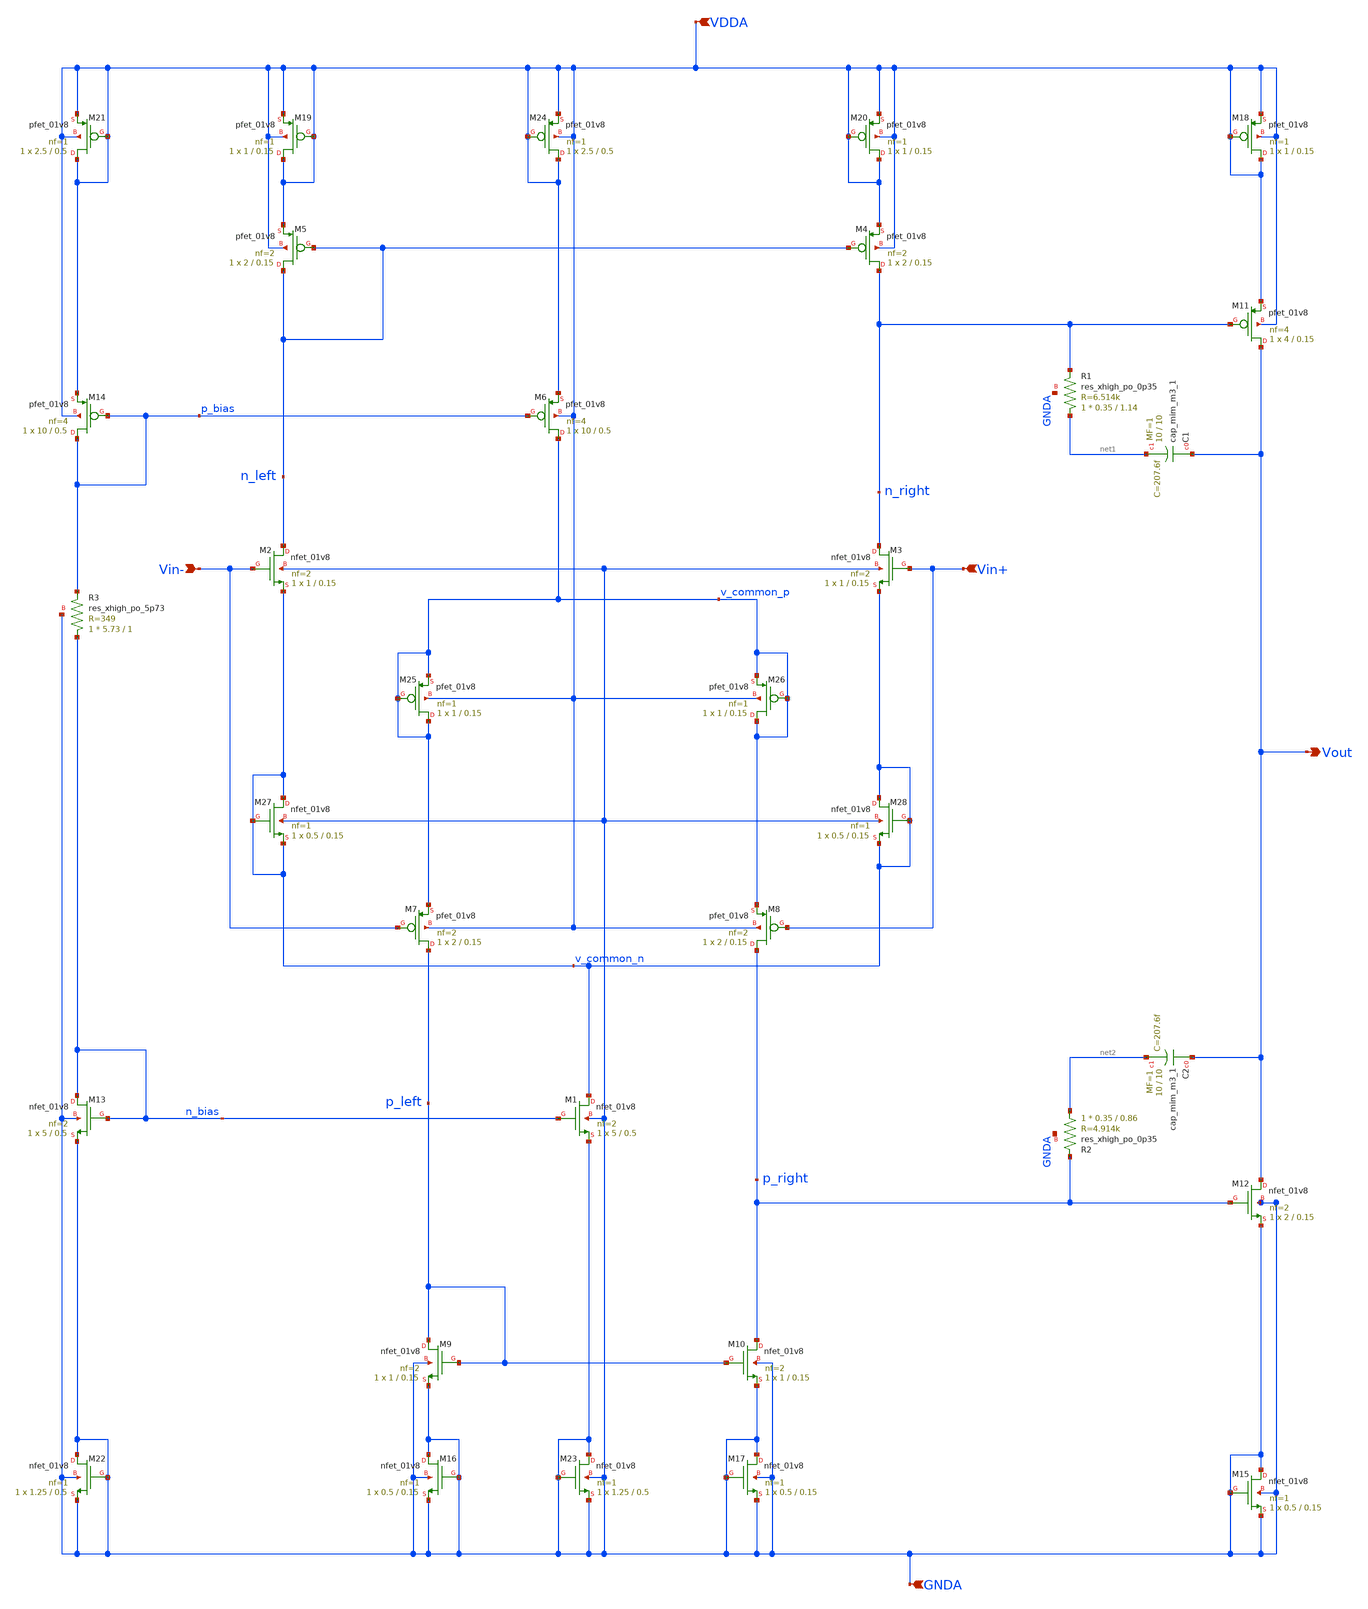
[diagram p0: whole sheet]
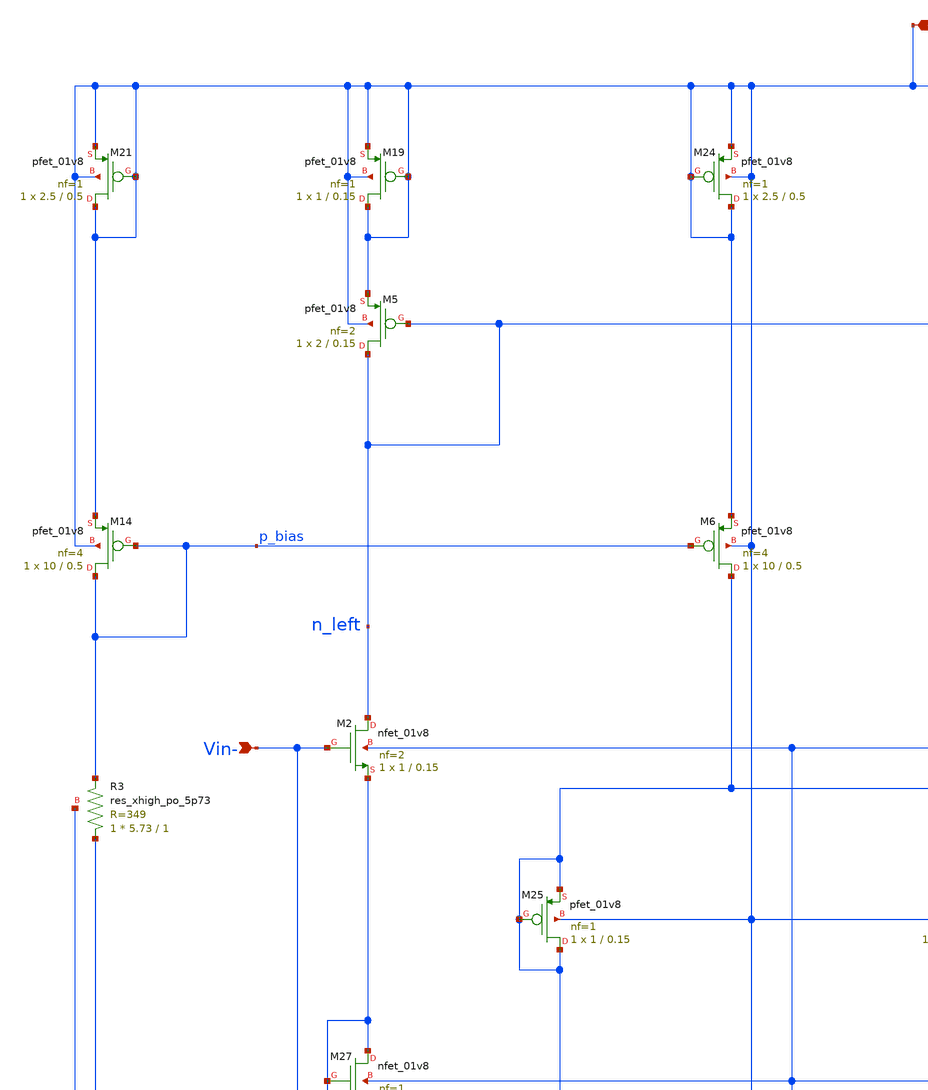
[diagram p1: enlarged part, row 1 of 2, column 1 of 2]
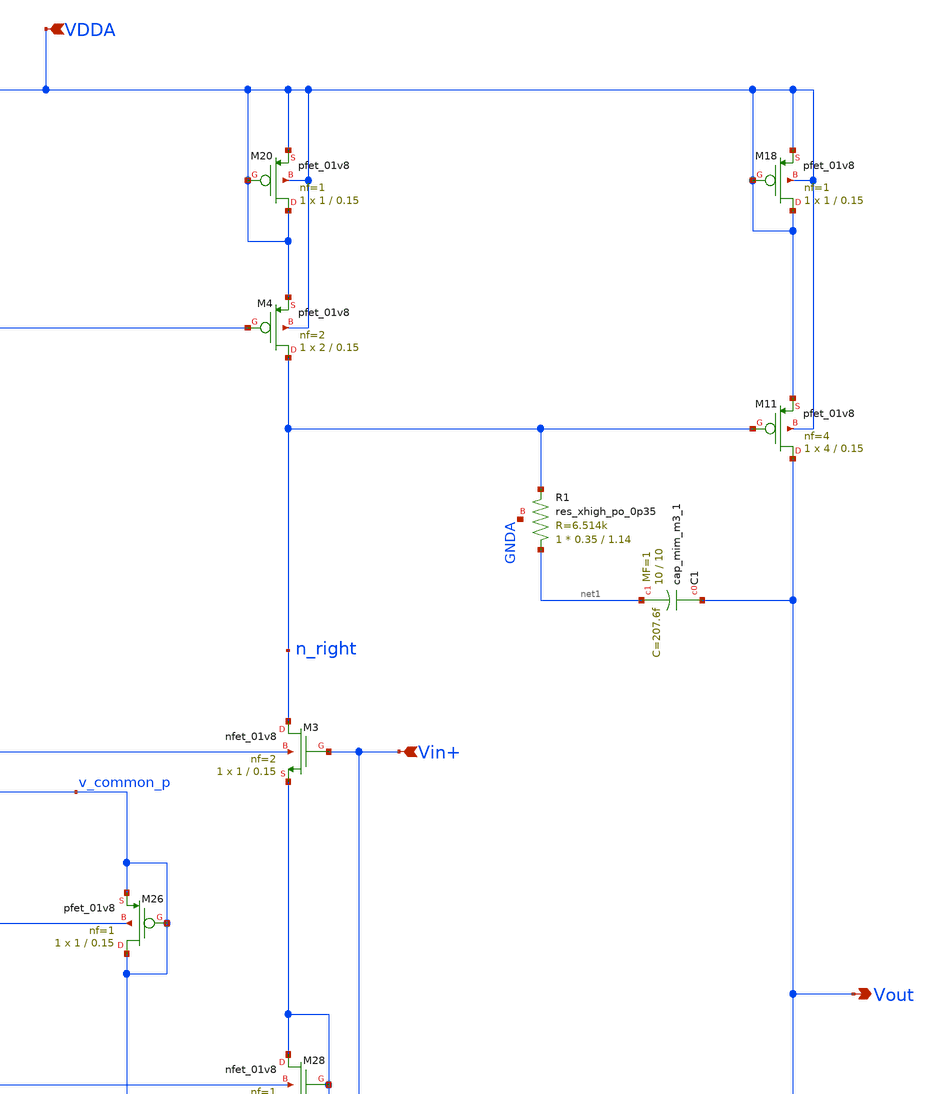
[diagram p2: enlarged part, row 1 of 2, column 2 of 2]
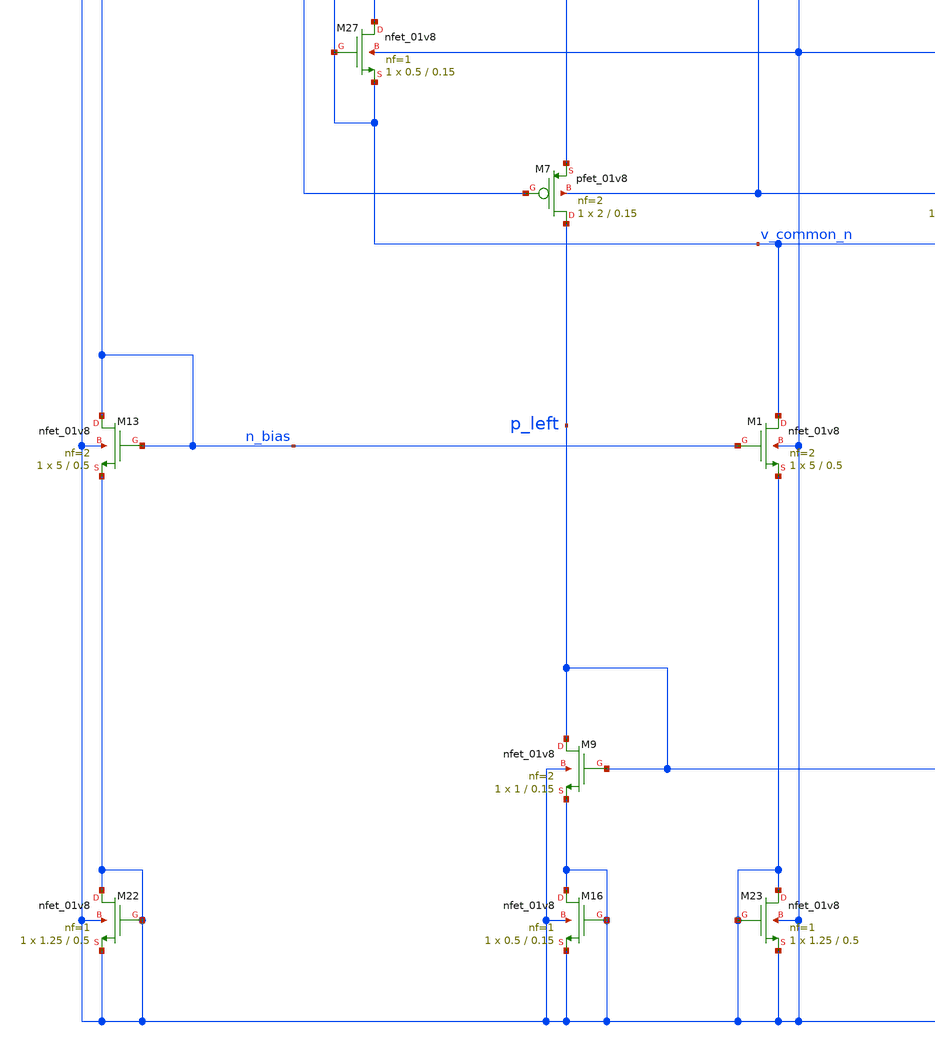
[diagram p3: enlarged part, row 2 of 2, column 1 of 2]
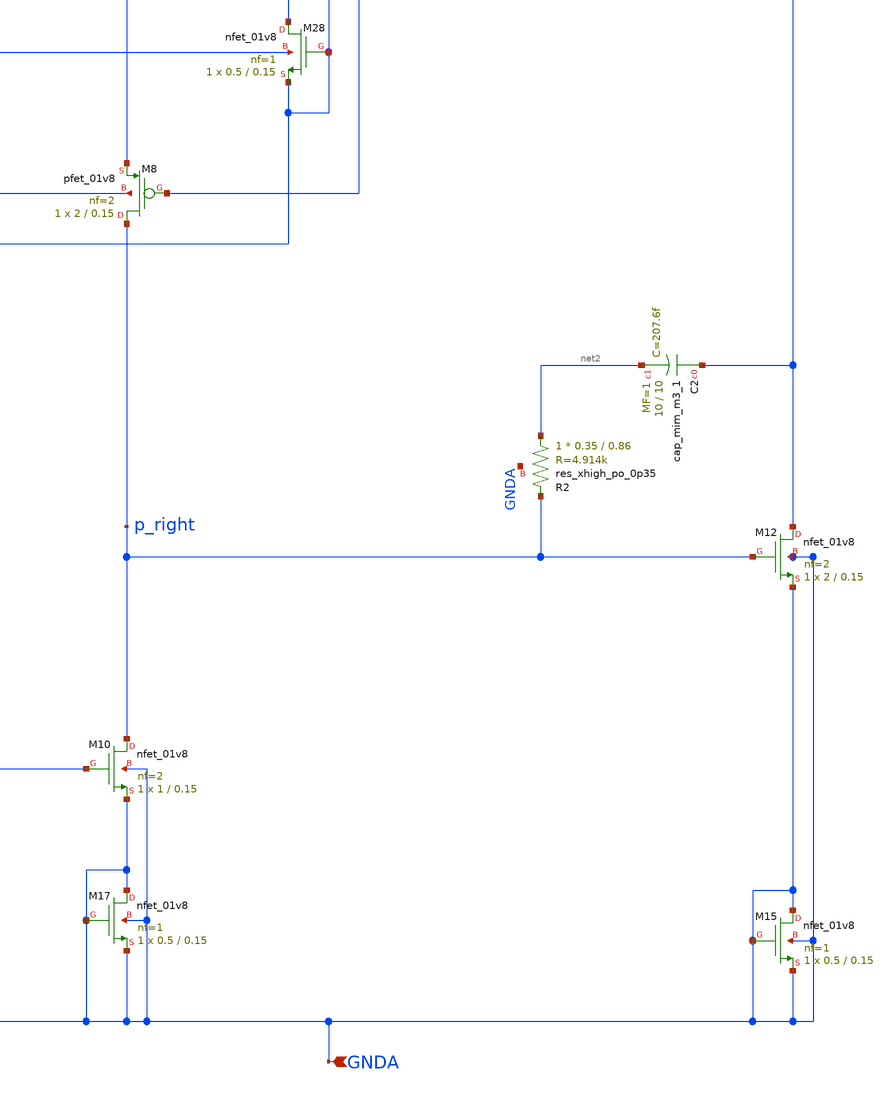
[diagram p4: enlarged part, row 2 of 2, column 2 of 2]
** sch_path: projects/pll/charge_pump/xschem_ngspice/rail_to_rail_opamp6_3.sch
**.subckt rail_to_rail_opamp6_3 Vout Vin+ Vin- VDDA GNDA
*.opin Vout
*.ipin Vin+
*.ipin Vin-
*.ipin VDDA
*.ipin GNDA
XM2 n_left Vin- v_common_n GNDA sky130_fd_pr__nfet_01v8 L=0.15 W=1 nf=2 ad='int((nf+1)/2) * W/nf * 0.29'
+ as='int((nf+2)/2) * W/nf * 0.29' pd='2*int((nf+1)/2) * (W/nf + 0.29)' ps='2*int((nf+2)/2) * (W/nf + 0.29)'
+ nrd='0.29 / W' nrs='0.29 / W' sa=0 sb=0 sd=0 mult=1 m=1
XM3 n_right Vin+ v_common_n GNDA sky130_fd_pr__nfet_01v8 L=0.15 W=1 nf=2 ad='int((nf+1)/2) * W/nf * 0.29'
+ as='int((nf+2)/2) * W/nf * 0.29' pd='2*int((nf+1)/2) * (W/nf + 0.29)' ps='2*int((nf+2)/2) * (W/nf + 0.29)'
+ nrd='0.29 / W' nrs='0.29 / W' sa=0 sb=0 sd=0 mult=1 m=1
XM5 n_left n_left VDDA VDDA sky130_fd_pr__pfet_01v8 L=0.15 W=2 nf=2 ad='int((nf+1)/2) * W/nf * 0.29'
+ as='int((nf+2)/2) * W/nf * 0.29' pd='2*int((nf+1)/2) * (W/nf + 0.29)' ps='2*int((nf+2)/2) * (W/nf + 0.29)'
+ nrd='0.29 / W' nrs='0.29 / W' sa=0 sb=0 sd=0 mult=1 m=1
XM4 n_right n_left VDDA VDDA sky130_fd_pr__pfet_01v8 L=0.15 W=2 nf=2 ad='int((nf+1)/2) * W/nf * 0.29'
+ as='int((nf+2)/2) * W/nf * 0.29' pd='2*int((nf+1)/2) * (W/nf + 0.29)' ps='2*int((nf+2)/2) * (W/nf + 0.29)'
+ nrd='0.29 / W' nrs='0.29 / W' sa=0 sb=0 sd=0 mult=1 m=1
XM6 v_common_p p_bias VDDA VDDA sky130_fd_pr__pfet_01v8 L=0.5 W=10 nf=4 ad='int((nf+1)/2) * W/nf * 0.29'
+ as='int((nf+2)/2) * W/nf * 0.29' pd='2*int((nf+1)/2) * (W/nf + 0.29)' ps='2*int((nf+2)/2) * (W/nf + 0.29)'
+ nrd='0.29 / W' nrs='0.29 / W' sa=0 sb=0 sd=0 mult=1 m=1
XM7 p_left Vin- v_common_p VDDA sky130_fd_pr__pfet_01v8 L=0.15 W=2 nf=2 ad='int((nf+1)/2) * W/nf * 0.29'
+ as='int((nf+2)/2) * W/nf * 0.29' pd='2*int((nf+1)/2) * (W/nf + 0.29)' ps='2*int((nf+2)/2) * (W/nf + 0.29)'
+ nrd='0.29 / W' nrs='0.29 / W' sa=0 sb=0 sd=0 mult=1 m=1
XM8 p_right Vin+ v_common_p VDDA sky130_fd_pr__pfet_01v8 L=0.15 W=2 nf=2 ad='int((nf+1)/2) * W/nf * 0.29'
+ as='int((nf+2)/2) * W/nf * 0.29' pd='2*int((nf+1)/2) * (W/nf + 0.29)' ps='2*int((nf+2)/2) * (W/nf + 0.29)'
+ nrd='0.29 / W' nrs='0.29 / W' sa=0 sb=0 sd=0 mult=1 m=1
XM9 p_left p_left GNDA GNDA sky130_fd_pr__nfet_01v8 L=0.15 W=1 nf=2 ad='int((nf+1)/2) * W/nf * 0.29'
+ as='int((nf+2)/2) * W/nf * 0.29' pd='2*int((nf+1)/2) * (W/nf + 0.29)' ps='2*int((nf+2)/2) * (W/nf + 0.29)'
+ nrd='0.29 / W' nrs='0.29 / W' sa=0 sb=0 sd=0 mult=1 m=1
XM10 p_right p_left GNDA GNDA sky130_fd_pr__nfet_01v8 L=0.15 W=1 nf=2 ad='int((nf+1)/2) * W/nf * 0.29'
+ as='int((nf+2)/2) * W/nf * 0.29' pd='2*int((nf+1)/2) * (W/nf + 0.29)' ps='2*int((nf+2)/2) * (W/nf + 0.29)'
+ nrd='0.29 / W' nrs='0.29 / W' sa=0 sb=0 sd=0 mult=1 m=1
XM1 v_common_n n_bias GNDA GNDA sky130_fd_pr__nfet_01v8 L=0.5 W=5 nf=2 ad='int((nf+1)/2) * W/nf * 0.29'
+ as='int((nf+2)/2) * W/nf * 0.29' pd='2*int((nf+1)/2) * (W/nf + 0.29)' ps='2*int((nf+2)/2) * (W/nf + 0.29)'
+ nrd='0.29 / W' nrs='0.29 / W' sa=0 sb=0 sd=0 mult=1 m=1
XM11 Vout n_right VDDA VDDA sky130_fd_pr__pfet_01v8 L=0.15 W=4 nf=4 ad='int((nf+1)/2) * W/nf * 0.29'
+ as='int((nf+2)/2) * W/nf * 0.29' pd='2*int((nf+1)/2) * (W/nf + 0.29)' ps='2*int((nf+2)/2) * (W/nf + 0.29)'
+ nrd='0.29 / W' nrs='0.29 / W' sa=0 sb=0 sd=0 mult=1 m=1
XM12 Vout p_right GNDA GNDA sky130_fd_pr__nfet_01v8 L=0.15 W=2 nf=2 ad='int((nf+1)/2) * W/nf * 0.29'
+ as='int((nf+2)/2) * W/nf * 0.29' pd='2*int((nf+1)/2) * (W/nf + 0.29)' ps='2*int((nf+2)/2) * (W/nf + 0.29)'
+ nrd='0.29 / W' nrs='0.29 / W' sa=0 sb=0 sd=0 mult=1 m=1
XM13 n_bias n_bias GNDA GNDA sky130_fd_pr__nfet_01v8 L=0.5 W=5 nf=2 ad='int((nf+1)/2) * W/nf * 0.29'
+ as='int((nf+2)/2) * W/nf * 0.29' pd='2*int((nf+1)/2) * (W/nf + 0.29)' ps='2*int((nf+2)/2) * (W/nf + 0.29)'
+ nrd='0.29 / W' nrs='0.29 / W' sa=0 sb=0 sd=0 mult=1 m=1
XM14 p_bias p_bias VDDA VDDA sky130_fd_pr__pfet_01v8 L=0.5 W=10 nf=4 ad='int((nf+1)/2) * W/nf * 0.29'
+ as='int((nf+2)/2) * W/nf * 0.29' pd='2*int((nf+1)/2) * (W/nf + 0.29)' ps='2*int((nf+2)/2) * (W/nf + 0.29)'
+ nrd='0.29 / W' nrs='0.29 / W' sa=0 sb=0 sd=0 mult=1 m=1
XC1 Vout net1 sky130_fd_pr__cap_mim_m3_1 W=10 L=10 MF=1 m=1
XC2 Vout net2 sky130_fd_pr__cap_mim_m3_1 W=10 L=10 MF=1 m=1
XR1 net1 n_right GNDA sky130_fd_pr__res_xhigh_po_0p35 L=1.14 mult=1 m=1
XR2 net2 p_right GNDA sky130_fd_pr__res_xhigh_po_0p35 L=0.86 mult=1 m=1
XR3 n_bias p_bias GNDA sky130_fd_pr__res_xhigh_po_5p73 L=1 mult=1 m=1
XM15 GNDA GNDA GNDA GNDA sky130_fd_pr__nfet_01v8 L=0.15 W=0.5 nf=1 ad='int((nf+1)/2) * W/nf * 0.29' as='int((nf+2)/2) * W/nf * 0.29'
+ pd='2*int((nf+1)/2) * (W/nf + 0.29)' ps='2*int((nf+2)/2) * (W/nf + 0.29)' nrd='0.29 / W' nrs='0.29 / W'
+ sa=0 sb=0 sd=0 mult=1 m=1
XM16 GNDA GNDA GNDA GNDA sky130_fd_pr__nfet_01v8 L=0.15 W=0.5 nf=1 ad='int((nf+1)/2) * W/nf * 0.29' as='int((nf+2)/2) * W/nf * 0.29'
+ pd='2*int((nf+1)/2) * (W/nf + 0.29)' ps='2*int((nf+2)/2) * (W/nf + 0.29)' nrd='0.29 / W' nrs='0.29 / W'
+ sa=0 sb=0 sd=0 mult=1 m=1
XM17 GNDA GNDA GNDA GNDA sky130_fd_pr__nfet_01v8 L=0.15 W=0.5 nf=1 ad='int((nf+1)/2) * W/nf * 0.29' as='int((nf+2)/2) * W/nf * 0.29'
+ pd='2*int((nf+1)/2) * (W/nf + 0.29)' ps='2*int((nf+2)/2) * (W/nf + 0.29)' nrd='0.29 / W' nrs='0.29 / W'
+ sa=0 sb=0 sd=0 mult=1 m=1
XM18 VDDA VDDA VDDA VDDA sky130_fd_pr__pfet_01v8 L=0.15 W=1 nf=1 ad='int((nf+1)/2) * W/nf * 0.29' as='int((nf+2)/2) * W/nf * 0.29'
+ pd='2*int((nf+1)/2) * (W/nf + 0.29)' ps='2*int((nf+2)/2) * (W/nf + 0.29)' nrd='0.29 / W' nrs='0.29 / W'
+ sa=0 sb=0 sd=0 mult=1 m=1
XM19 VDDA VDDA VDDA VDDA sky130_fd_pr__pfet_01v8 L=0.15 W=1 nf=1 ad='int((nf+1)/2) * W/nf * 0.29' as='int((nf+2)/2) * W/nf * 0.29'
+ pd='2*int((nf+1)/2) * (W/nf + 0.29)' ps='2*int((nf+2)/2) * (W/nf + 0.29)' nrd='0.29 / W' nrs='0.29 / W'
+ sa=0 sb=0 sd=0 mult=1 m=1
XM20 VDDA VDDA VDDA VDDA sky130_fd_pr__pfet_01v8 L=0.15 W=1 nf=1 ad='int((nf+1)/2) * W/nf * 0.29' as='int((nf+2)/2) * W/nf * 0.29'
+ pd='2*int((nf+1)/2) * (W/nf + 0.29)' ps='2*int((nf+2)/2) * (W/nf + 0.29)' nrd='0.29 / W' nrs='0.29 / W'
+ sa=0 sb=0 sd=0 mult=1 m=1
XM21 VDDA VDDA VDDA VDDA sky130_fd_pr__pfet_01v8 L=0.5 W=2.5 nf=1 ad='int((nf+1)/2) * W/nf * 0.29' as='int((nf+2)/2) * W/nf * 0.29'
+ pd='2*int((nf+1)/2) * (W/nf + 0.29)' ps='2*int((nf+2)/2) * (W/nf + 0.29)' nrd='0.29 / W' nrs='0.29 / W'
+ sa=0 sb=0 sd=0 mult=1 m=1
XM22 GNDA GNDA GNDA GNDA sky130_fd_pr__nfet_01v8 L=0.5 W=1.25 nf=1 ad='int((nf+1)/2) * W/nf * 0.29' as='int((nf+2)/2) * W/nf * 0.29'
+ pd='2*int((nf+1)/2) * (W/nf + 0.29)' ps='2*int((nf+2)/2) * (W/nf + 0.29)' nrd='0.29 / W' nrs='0.29 / W'
+ sa=0 sb=0 sd=0 mult=1 m=1
XM23 GNDA GNDA GNDA GNDA sky130_fd_pr__nfet_01v8 L=0.5 W=1.25 nf=1 ad='int((nf+1)/2) * W/nf * 0.29' as='int((nf+2)/2) * W/nf * 0.29'
+ pd='2*int((nf+1)/2) * (W/nf + 0.29)' ps='2*int((nf+2)/2) * (W/nf + 0.29)' nrd='0.29 / W' nrs='0.29 / W'
+ sa=0 sb=0 sd=0 mult=1 m=1
XM24 VDDA VDDA VDDA VDDA sky130_fd_pr__pfet_01v8 L=0.5 W=2.5 nf=1 ad='int((nf+1)/2) * W/nf * 0.29' as='int((nf+2)/2) * W/nf * 0.29'
+ pd='2*int((nf+1)/2) * (W/nf + 0.29)' ps='2*int((nf+2)/2) * (W/nf + 0.29)' nrd='0.29 / W' nrs='0.29 / W'
+ sa=0 sb=0 sd=0 mult=1 m=1
XM25 v_common_p v_common_p v_common_p VDDA sky130_fd_pr__pfet_01v8 L=0.15 W=1 nf=1 ad='int((nf+1)/2) * W/nf * 0.29'
+ as='int((nf+2)/2) * W/nf * 0.29' pd='2*int((nf+1)/2) * (W/nf + 0.29)' ps='2*int((nf+2)/2) * (W/nf + 0.29)'
+ nrd='0.29 / W' nrs='0.29 / W' sa=0 sb=0 sd=0 mult=1 m=1
XM26 v_common_p v_common_p v_common_p VDDA sky130_fd_pr__pfet_01v8 L=0.15 W=1 nf=1 ad='int((nf+1)/2) * W/nf * 0.29'
+ as='int((nf+2)/2) * W/nf * 0.29' pd='2*int((nf+1)/2) * (W/nf + 0.29)' ps='2*int((nf+2)/2) * (W/nf + 0.29)'
+ nrd='0.29 / W' nrs='0.29 / W' sa=0 sb=0 sd=0 mult=1 m=1
XM27 v_common_n v_common_n v_common_n GNDA sky130_fd_pr__nfet_01v8 L=0.15 W=0.5 nf=1 ad='int((nf+1)/2) * W/nf * 0.29'
+ as='int((nf+2)/2) * W/nf * 0.29' pd='2*int((nf+1)/2) * (W/nf + 0.29)' ps='2*int((nf+2)/2) * (W/nf + 0.29)'
+ nrd='0.29 / W' nrs='0.29 / W' sa=0 sb=0 sd=0 mult=1 m=1
XM28 v_common_n v_common_n v_common_n GNDA sky130_fd_pr__nfet_01v8 L=0.15 W=0.5 nf=1 ad='int((nf+1)/2) * W/nf * 0.29'
+ as='int((nf+2)/2) * W/nf * 0.29' pd='2*int((nf+1)/2) * (W/nf + 0.29)' ps='2*int((nf+2)/2) * (W/nf + 0.29)'
+ nrd='0.29 / W' nrs='0.29 / W' sa=0 sb=0 sd=0 mult=1 m=1
**.ends
.end
